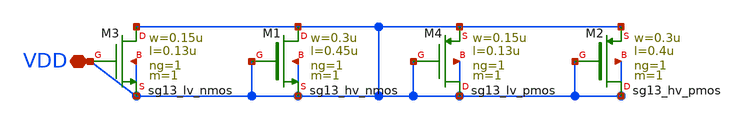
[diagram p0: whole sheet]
** sch_path: ihp-sg13g2/schematic/xschem/sg13_short1.sch
**.subckt sg13_short1 VDD
*.iopin VDD
XM1 VDD VDD VDD VDD sg13_hv_nmos w=0.3u l=0.45u ng=1 m=1 mm_ok=1
XM2 VDD VDD VDD VDD sg13_hv_pmos w=0.3u l=0.4u ng=1 m=1 mm_ok=1
XM3 VDD VDD VDD VDD sg13_lv_nmos w=0.15u l=0.13u ng=1 m=1 mm_ok=1
XM4 VDD VDD VDD VDD sg13_lv_pmos w=0.15u l=0.13u ng=1 m=1 mm_ok=1
**.ends
.end
